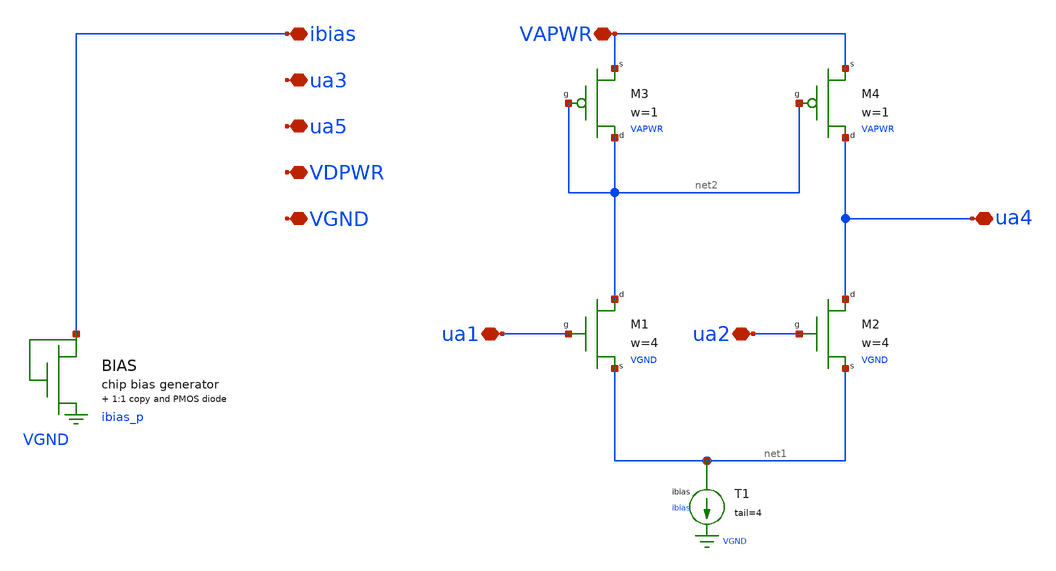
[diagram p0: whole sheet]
** sch_path: examples/diffamp/diffamp.sch
**.subckt diffamp ibias ua1 ua2 ua3 ua4 ua5 VAPWR VDPWR VGND
*.iopin ibias
*.iopin ua1
*.iopin ua2
*.iopin ua3
*.iopin ua4
*.iopin ua5
*.iopin VAPWR
*.iopin VDPWR
*.iopin VGND
XM1 ua1 net2 net1 VGND mosbius_nmos w=4
XM2 ua2 ua4 net1 VGND mosbius_nmos w=4
XT1 net1 ibias VGND mosbius_ntail tail=4
M3 net2 net2 VAPWR VAPWR mosbius_pmos w=1
M4 net2 ua4 VAPWR VAPWR mosbius_pmos w=1
XBIAS ibias ibias_p VGND VAPWR mosbius_bias
**.ends

* expanding   symbol:  mosbius_nmos.sym # of pins=3
** sym_path: xschem/mosbius_lib/mosbius_nmos.sym
** sch_path: xschem/mosbius_lib/mosbius_nmos.sch
.subckt mosbius_nmos g d s b  w=1
*.iopin s
*.ipin g
*.iopin d
XM1 d g s well sky130_fd_pr__nfet_g5v0d10v5 L=0.5 W=wdev nf=nfdev ad='int((nf+1)/2) * W/nf * 0.29' as='int((nf+2)/2) * W/nf * 0.29'
+ pd='2*int((nf+1)/2) * (W/nf + 0.29)' ps='2*int((nf+2)/2) * (W/nf + 0.29)' nrd='0.29 / W' nrs='0.29 / W'
+ sa=0 sb=0 sd=0 mult=1 m=1
**** begin user architecture code

.param wdev='10*w' nfdev='2*w'

**** end user architecture code
Rwell_source well s 'rwell_source' m=1
Rwell_rail well b 'rwell_rail' m=1
* implicit port xxx
.ends


* expanding   symbol:  mosbius_ntail.sym # of pins=1
** sym_path: xschem/mosbius_lib/mosbius_ntail.sym
** sch_path: xschem/mosbius_lib/mosbius_ntail.sch
.subckt mosbius_ntail d g s  tail=2
*.iopin d
XM2 d g s s sky130_fd_pr__nfet_g5v0d10v5 L=1 W=20*(tail/2) nf=4*(tail/2) ad='int((nf+1)/2) * W/nf * 0.29'
+ as='int((nf+2)/2) * W/nf * 0.29' pd='2*int((nf+1)/2) * (W/nf + 0.29)' ps='2*int((nf+2)/2) * (W/nf + 0.29)'
+ nrd='0.29 / W' nrs='0.29 / W' sa=0 sb=0 sd=0 mult=1 m=1
* implicit port g
* implicit port s
.ends


* expanding   symbol:  mosbius_pmos.sym # of pins=3
** sym_path: xschem/mosbius_lib/mosbius_pmos.sym
** sch_path: xschem/mosbius_lib/mosbius_pmos.sch
.subckt mosbius_pmos g d s b  w=1
*.iopin s
*.ipin g
*.iopin d
XM1 d g s well sky130_fd_pr__pfet_g5v0d10v5 L=0.5 W=wdev nf=nfdev ad='int((nf+1)/2) * W/nf * 0.29' as='int((nf+2)/2) * W/nf * 0.29'
+ pd='2*int((nf+1)/2) * (W/nf + 0.29)' ps='2*int((nf+2)/2) * (W/nf + 0.29)' nrd='0.29 / W' nrs='0.29 / W'
+ sa=0 sb=0 sd=0 mult=1 m=1
**** begin user architecture code

.param wdev='30*w' nfdev='wdev/pmos_width_per_finger'

**** end user architecture code
Rwell_source well s 'rwell_source' m=1
Rwell_rail well b 'rwell_rail' m=1
* implicit port xxx
.ends


* expanding   symbol:  mosbius_bias.sym # of pins=1
** sym_path: xschem/mosbius_lib/mosbius_bias.sym
** sch_path: xschem/mosbius_lib/mosbius_bias.sch
.subckt mosbius_bias ibias ibias_p bn bp
*.iopin ibias
XMbias_ref ibias ibias bn bn sky130_fd_pr__nfet_g5v0d10v5 L=1 W=10 nf=2 ad='int((nf+1)/2) * W/nf * 0.29'
+ as='int((nf+2)/2) * W/nf * 0.29' pd='2*int((nf+1)/2) * (W/nf + 0.29)' ps='2*int((nf+2)/2) * (W/nf + 0.29)'
+ nrd='0.29 / W' nrs='0.29 / W' sa=0 sb=0 sd=0 mult=1 m=1
XMbias_copy ibias_p ibias bn bn sky130_fd_pr__nfet_g5v0d10v5 L=1 W=10 nf=2 ad='int((nf+1)/2) * W/nf * 0.29'
+ as='int((nf+2)/2) * W/nf * 0.29' pd='2*int((nf+1)/2) * (W/nf + 0.29)' ps='2*int((nf+2)/2) * (W/nf + 0.29)'
+ nrd='0.29 / W' nrs='0.29 / W' sa=0 sb=0 sd=0 mult=1 m=1
XMbias_p ibias_p ibias_p bp bp sky130_fd_pr__pfet_g5v0d10v5 L=1 W=30 nf=30/pmos_width_per_finger ad='int((nf+1)/2) * W/nf * 0.29'
+ as='int((nf+2)/2) * W/nf * 0.29' pd='2*int((nf+1)/2) * (W/nf + 0.29)' ps='2*int((nf+2)/2) * (W/nf + 0.29)'
+ nrd='0.29 / W' nrs='0.29 / W' sa=0 sb=0 sd=0 mult=1 m=1
* implicit port xxx
.ends

.end
